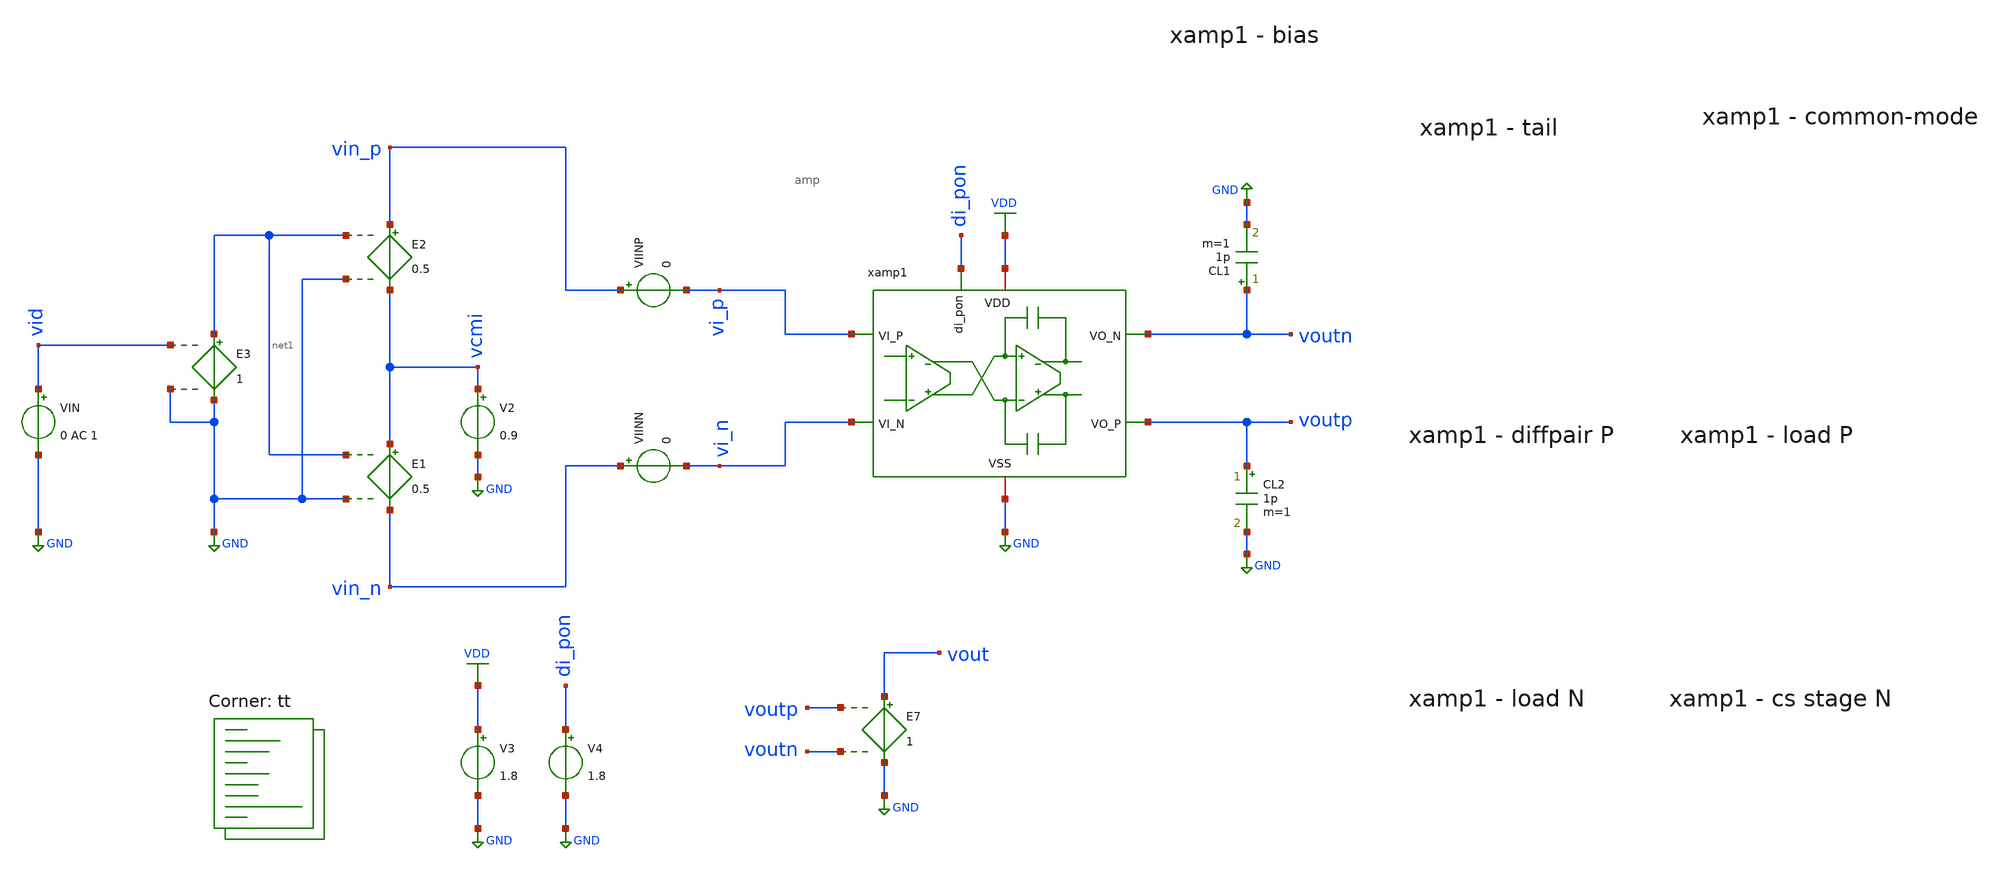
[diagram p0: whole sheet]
** sch_path: xschem/tb_amp_ol.sch
**.subckt tb_amp_ol
V3 VDD GND 1.8
V2 vcmi GND 0.9
E1 vcmi vin_n net1 GND 0.5
E2 vin_p vcmi net1 GND 0.5
VIN vid GND 0 AC 1
E3 net1 GND vid GND 1
VIINP vin_p vi_p 0
VIINN vin_n vi_n 0
V4 di_pon GND 1.8
E7 vout GND voutp voutn 1
CL2 voutp GND 1p m=1
xamp1 VDD vi_n vi_p voutp di_pon voutn GND amp
CL1 voutn GND 1p m=1
**** begin user architecture code
.lib $::SKYWATER_MODELS/sky130.lib.spice tt


.include /foss/designs/xschem/amp_dev_sav.spice
.options savecurrents

.save all
.control
set doAmpSim = 1
set doNoise = 0

	setplot const
	let f_min = 10
	let f_max = 1G
	let f_stop = 500k

	let Adc = 220
	let v_step_o = 0.9
	let v_step_i = -v_step_o/Adc

	let t_rf = 0.01u
	let t_step = 5u
	let t_delay = 0
	let t_per = 2*t_step

	let tstep = 0.001*t_step
	let tstop = 2*t_per
	let tstart = t_delay

	alter @VIN[DC] = 0.0
	alter @VIN[PULSE] = [ 0 $&v_step_i $&t_delay $&t_rf $&t_rf $&t_step $&t_per 0 ]

if $doAmpSim eq 1

alter @m.xamp1.xmn1.msky130_fd_pr__nfet_01v8[nf] = 4 # load N
alter @m.xamp1.xmn2.msky130_fd_pr__nfet_01v8[nf] = @m.xamp1.xmn1.msky130_fd_pr__nfet_01v8[nf]

alter @m.xamp1.xmp4.msky130_fd_pr__pfet_01v8[nf] = 50 # diffpair P
alter @m.xamp1.xmp5.msky130_fd_pr__pfet_01v8[nf] = @m.xamp1.xmp4.msky130_fd_pr__pfet_01v8[nf]

alter @m.xamp1.xmp6.msky130_fd_pr__pfet_01v8[nf] = 1 # load P
alter @m.xamp1.xmp7.msky130_fd_pr__pfet_01v8[nf] = @m.xamp1.xmp6.msky130_fd_pr__pfet_01v8[nf]

alter @m.xamp1.xmn3.msky130_fd_pr__nfet_01v8[nf] = 1 # cs stage N
alter @m.xamp1.xmn4.msky130_fd_pr__nfet_01v8[nf] = @m.xamp1.xmn3.msky130_fd_pr__nfet_01v8[nf]

	ac dec 100 $&const.f_min $&const.f_max

	setplot ac1
	let Atot = v(vout)/v(vid)

	let Amag_ol_dB = vdb(Atot)
	let Aarg_ol = 180/PI*cphase(Atot)

	**let Amag_ol_dB_1 = vdb(A1)
	**let Aarg_ol_1 = 180/PI*cphase(A1)

	**let Amag_ol_dB_2 = vdb(A2)
	**let Aarg_ol_2 = 180/PI*cphase(A2)

	meas ac Adc_ol_dB max Amag_ol_dB
	let Amag_fc = Adc_ol_dB-3

	meas ac fc find frequency when Amag_ol_dB = Amag_fc
#	meas ac fug_ol find frequency when Amag_ol_dB=0
#	meas ac pm find Aarg_ol when frequency=fug_ol
#	let pm = 180 + pm
#	print pm

	let Adc_ol_lin = 10^(Adc_ol_dB/20)
	let err_gain = 1-Adc_ol_lin/(1+Adc_ol_lin)
#	print err_gain*100

#	plot Amag_ol_dB Aarg_ol ylabel 'Open Loop Magnitude, Phase'

end

if $doNoise eq 1

	noise v(vout) vin dec 100 $&const.f_min $&const.f_max

	tran $&tstep $&tstop $&tstart

	setplot noise1
	let acgain = onoise_spectrum/inoise_spectrum
	plot onoise_spectrum ylog xlog ylabel 'Output Noise'
	*plot acgain

	setplot noise2
	print onoise_total

	setplot tran2
	let vcmo = (v(voutp)+v(voutn))/2
	plot v(vin_p) v(vin_n) v(voutp) v(voutn) vcmo
end

reset
op


*rm /foss/designs/filter/dc.txt
*show >> /foss/designs/filter/dc.txt
remzerovec
write tb_amp_ol.raw
.endc

**** end user architecture code
**.ends
.GLOBAL GND
.GLOBAL VDD
.end
